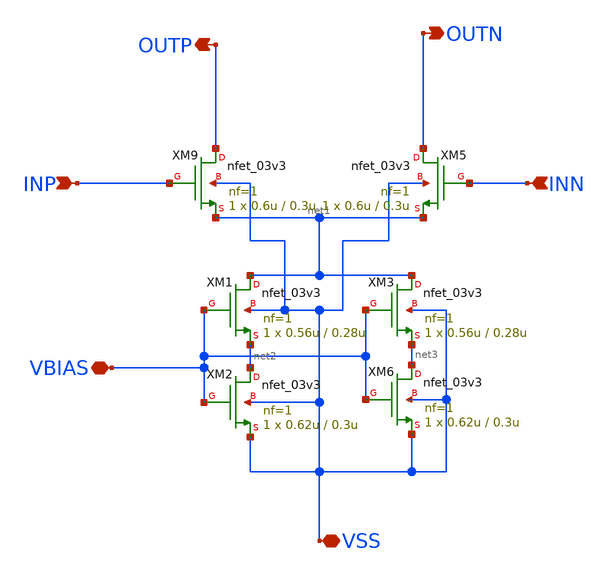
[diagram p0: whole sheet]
** sch_path: xschem/CS_Switch_16x2.sch
**.subckt CS_Switch_16x2 INP INN OUTP OUTN VBIAS VSS
*.ipin INP
*.ipin INN
*.opin OUTP
*.opin OUTN
*.iopin VBIAS
*.iopin VSS
XM2 net2 VBIAS VSS VSS nfet_03v3 L=0.3u W=0.62u nf=1 ad='int((nf+1)/2) * W/nf * 0.18u' as='int((nf+2)/2) * W/nf * 0.18u'
+ pd='2*int((nf+1)/2) * (W/nf + 0.18u)' ps='2*int((nf+2)/2) * (W/nf + 0.18u)' nrd='0.18u / W' nrs='0.18u / W'
+ sa=0 sb=0 sd=0 m=1
XM1 net1 VBIAS net2 VSS nfet_03v3 L=0.28u W=0.56u nf=1 ad='int((nf+1)/2) * W/nf * 0.18u' as='int((nf+2)/2) * W/nf * 0.18u'
+ pd='2*int((nf+1)/2) * (W/nf + 0.18u)' ps='2*int((nf+2)/2) * (W/nf + 0.18u)' nrd='0.18u / W' nrs='0.18u / W'
+ sa=0 sb=0 sd=0 m=1
XM3 net1 VBIAS net3 VSS nfet_03v3 L=0.28u W=0.56u nf=1 ad='int((nf+1)/2) * W/nf * 0.18u' as='int((nf+2)/2) * W/nf * 0.18u'
+ pd='2*int((nf+1)/2) * (W/nf + 0.18u)' ps='2*int((nf+2)/2) * (W/nf + 0.18u)' nrd='0.18u / W' nrs='0.18u / W'
+ sa=0 sb=0 sd=0 m=1
XM5 OUTN INN net1 VSS nfet_03v3 L=0.3u W=0.6u nf=1 ad='int((nf+1)/2) * W/nf * 0.18u' as='int((nf+2)/2) * W/nf * 0.18u'
+ pd='2*int((nf+1)/2) * (W/nf + 0.18u)' ps='2*int((nf+2)/2) * (W/nf + 0.18u)' nrd='0.18u / W' nrs='0.18u / W'
+ sa=0 sb=0 sd=0 m=1
XM6 net3 VBIAS VSS VSS nfet_03v3 L=0.3u W=0.62u nf=1 ad='int((nf+1)/2) * W/nf * 0.18u' as='int((nf+2)/2) * W/nf * 0.18u'
+ pd='2*int((nf+1)/2) * (W/nf + 0.18u)' ps='2*int((nf+2)/2) * (W/nf + 0.18u)' nrd='0.18u / W' nrs='0.18u / W'
+ sa=0 sb=0 sd=0 m=1
XM9 OUTP INP net1 VSS nfet_03v3 L=0.3u W=0.6u nf=1 ad='int((nf+1)/2) * W/nf * 0.18u' as='int((nf+2)/2) * W/nf * 0.18u'
+ pd='2*int((nf+1)/2) * (W/nf + 0.18u)' ps='2*int((nf+2)/2) * (W/nf + 0.18u)' nrd='0.18u / W' nrs='0.18u / W'
+ sa=0 sb=0 sd=0 m=1
**.ends
.end
